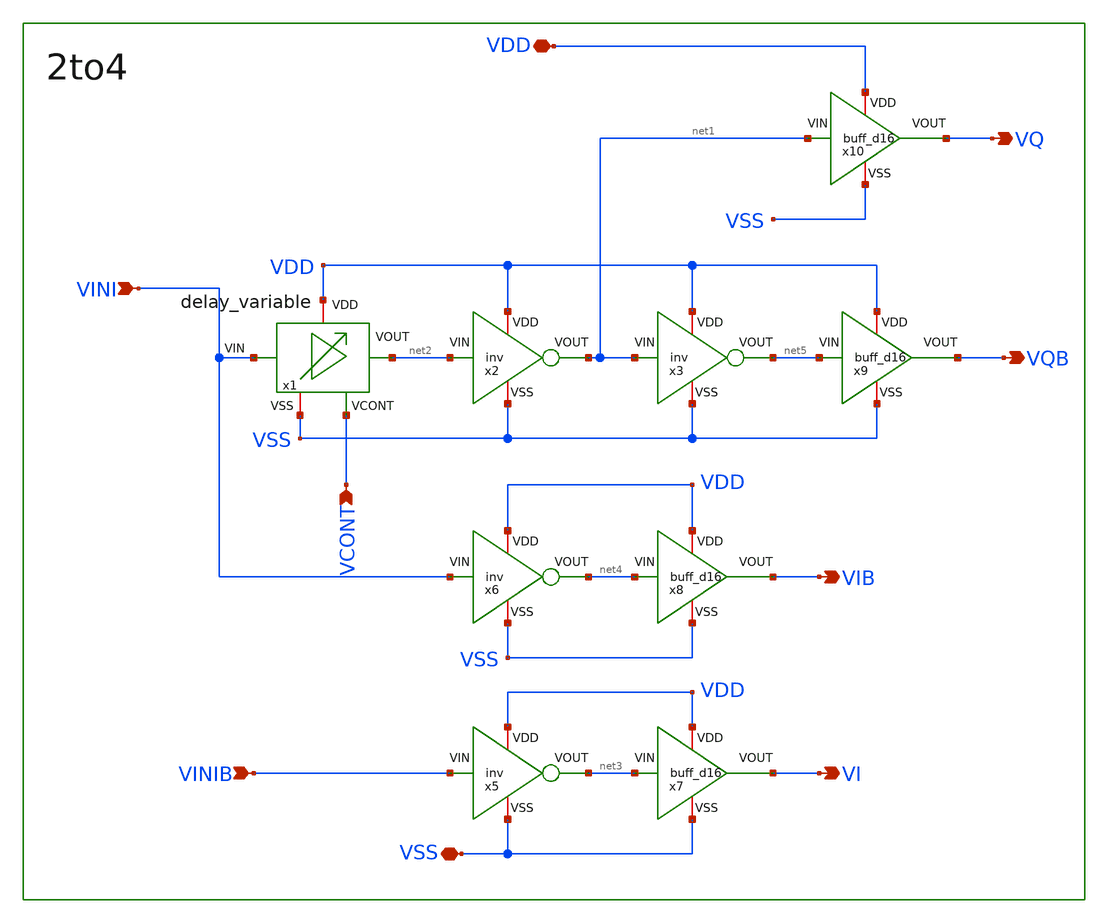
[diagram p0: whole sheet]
** sch_path: 2to4/2to4prelim.sch
**.subckt 2to4prelim VDD VSS VCONT VINI VIB VQ VQB VINIB VI
*.iopin VDD
*.iopin VSS
*.ipin VCONT
*.ipin VINI
*.opin VIB
*.opin VQ
*.opin VQB
*.ipin VINIB
*.opin VI
x1 VDD VINI net2 VCONT VSS delay_variable
x2 VDD net1 net2 VSS inv
x3 VDD net5 net1 VSS inv
x6 VDD net4 VINI VSS inv
x5 VDD net3 VINIB VSS inv
x7 VDD VI net3 VSS buff_d16
x8 VDD VIB net4 VSS buff_d16
x9 VDD VQB net5 VSS buff_d16
x10 VDD VQ net1 VSS buff_d16
**.ends
.end
